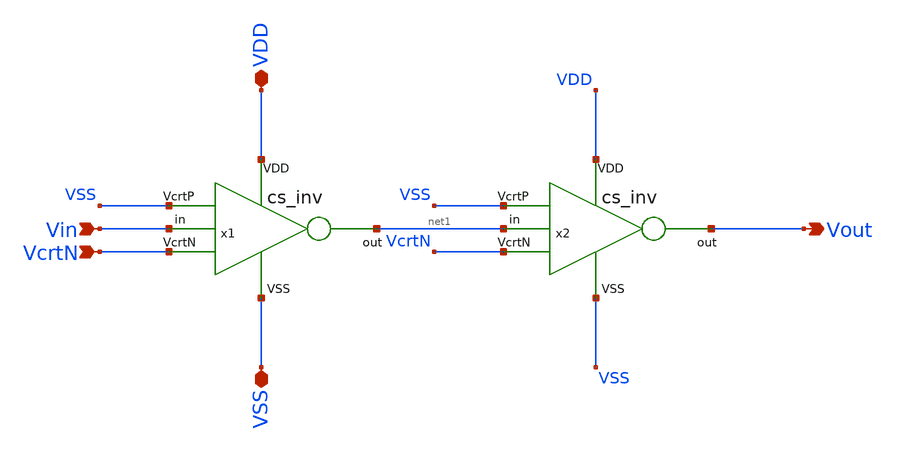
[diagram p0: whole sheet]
** sch_path: work/comparator_inv/xschem/comparator_cs_inv.sch
**.subckt comparator_cs_inv Vout VSS VDD Vin VcrtN
*.opin Vout
*.iopin VSS
*.iopin VDD
*.ipin Vin
*.ipin VcrtN
x1 VDD VSS Vin net1 VcrtN VSS cs_inv
x2 VDD VSS net1 Vout VcrtN VSS cs_inv
**.ends

* expanding   symbol:  /foss/designs/chipathon_2025/designs/ihp-sg13g2/gate_cs_inv/xschem/cs_inv.sym
*+ # of pins=6
** sym_path: /foss/designs/chipathon_2025/designs/ihp-sg13g2/gate_cs_inv/xschem/cs_inv.sym
** sch_path: /foss/designs/chipathon_2025/designs/ihp-sg13g2/gate_cs_inv/xschem/cs_inv.sch
.subckt cs_inv VDD VcrtP in out VcrtN VSS
*.ipin VDD
*.ipin VSS
*.ipin in
*.opin out
*.ipin VcrtP
*.ipin VcrtN
XM1 out in net2 VSS sg13_lv_nmos w=1.0u l=0.13u ng=1 m=1 mm_ok=1
XM2 net2 VcrtN VSS VSS sg13_lv_nmos w={WCrtN} l=0.13u ng=1 m=1 mm_ok=1
XM3 net1 in out VDD sg13_lv_pmos w=2u l=0.13u ng=1 m=1 mm_ok=1
XM4 VDD VcrtP net1 VDD sg13_lv_pmos w=2u l=0.13u ng=1 m=1 mm_ok=1
.ends

.end
